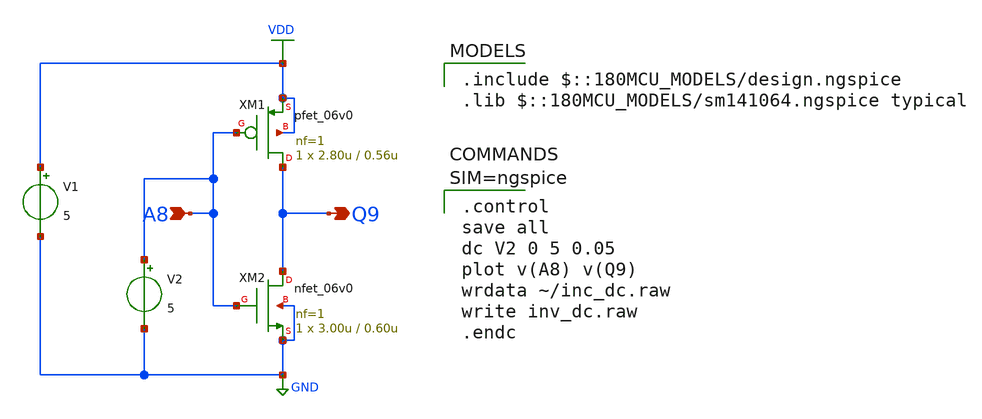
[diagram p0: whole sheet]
** sch_path: member_project/homelith/inverter/xschem/inv_with_sim.sch
* Copyright 2022 GlobalFoundries PDK Authors
* Licensed under the Apache License, Version 2.0 (the "License");
* you may not use this file except in compliance with the License.
* You may obtain a copy of the License at
* https://www.apache.org/licenses/LICENSE-2.0
* Unless required by applicable law or agreed to in writing, software
* distributed under the License is distributed on an "AS IS" BASIS,
* WITHOUT WARRANTIES OR CONDITIONS OF ANY KIND, either express or implied.
* See the License for the specific language governing permissions and
* limitations under the License.
**.subckt inv_with_sim A8 Q9
*.ipin A8
*.opin Q9
V1 VDD GND 5
V2 A8 GND 5
XM1 Q9 A8 VDD VDD pfet_06v0 L=0.56u W=2.80u nf=1 ad='int((nf+1)/2) * W/nf * 0.18u' as='int((nf+2)/2) * W/nf * 0.18u'
+ pd='2*int((nf+1)/2) * (W/nf + 0.18u)' ps='2*int((nf+2)/2) * (W/nf + 0.18u)' nrd='0.18u / W' nrs='0.18u / W'
+ sa=0 sb=0 sd=0 m=1
XM2 Q9 A8 GND GND nfet_06v0 L=0.60u W=3.00u nf=1 ad='int((nf+1)/2) * W/nf * 0.18u' as='int((nf+2)/2) * W/nf * 0.18u'
+ pd='2*int((nf+1)/2) * (W/nf + 0.18u)' ps='2*int((nf+2)/2) * (W/nf + 0.18u)' nrd='0.18u / W' nrs='0.18u / W'
+ sa=0 sb=0 sd=0 m=1
**** begin user architecture code
 .include $::180MCU_MODELS/design.ngspice
.lib $::180MCU_MODELS/sm141064.ngspice typical


.control
save all
dc V2 0 5 0.05
plot v(A8) v(Q9)
wrdata ~/inc_dc.raw
write inv_dc.raw
.endc



**** end user architecture code
**.ends
.GLOBAL VDD
.GLOBAL GND
.end
